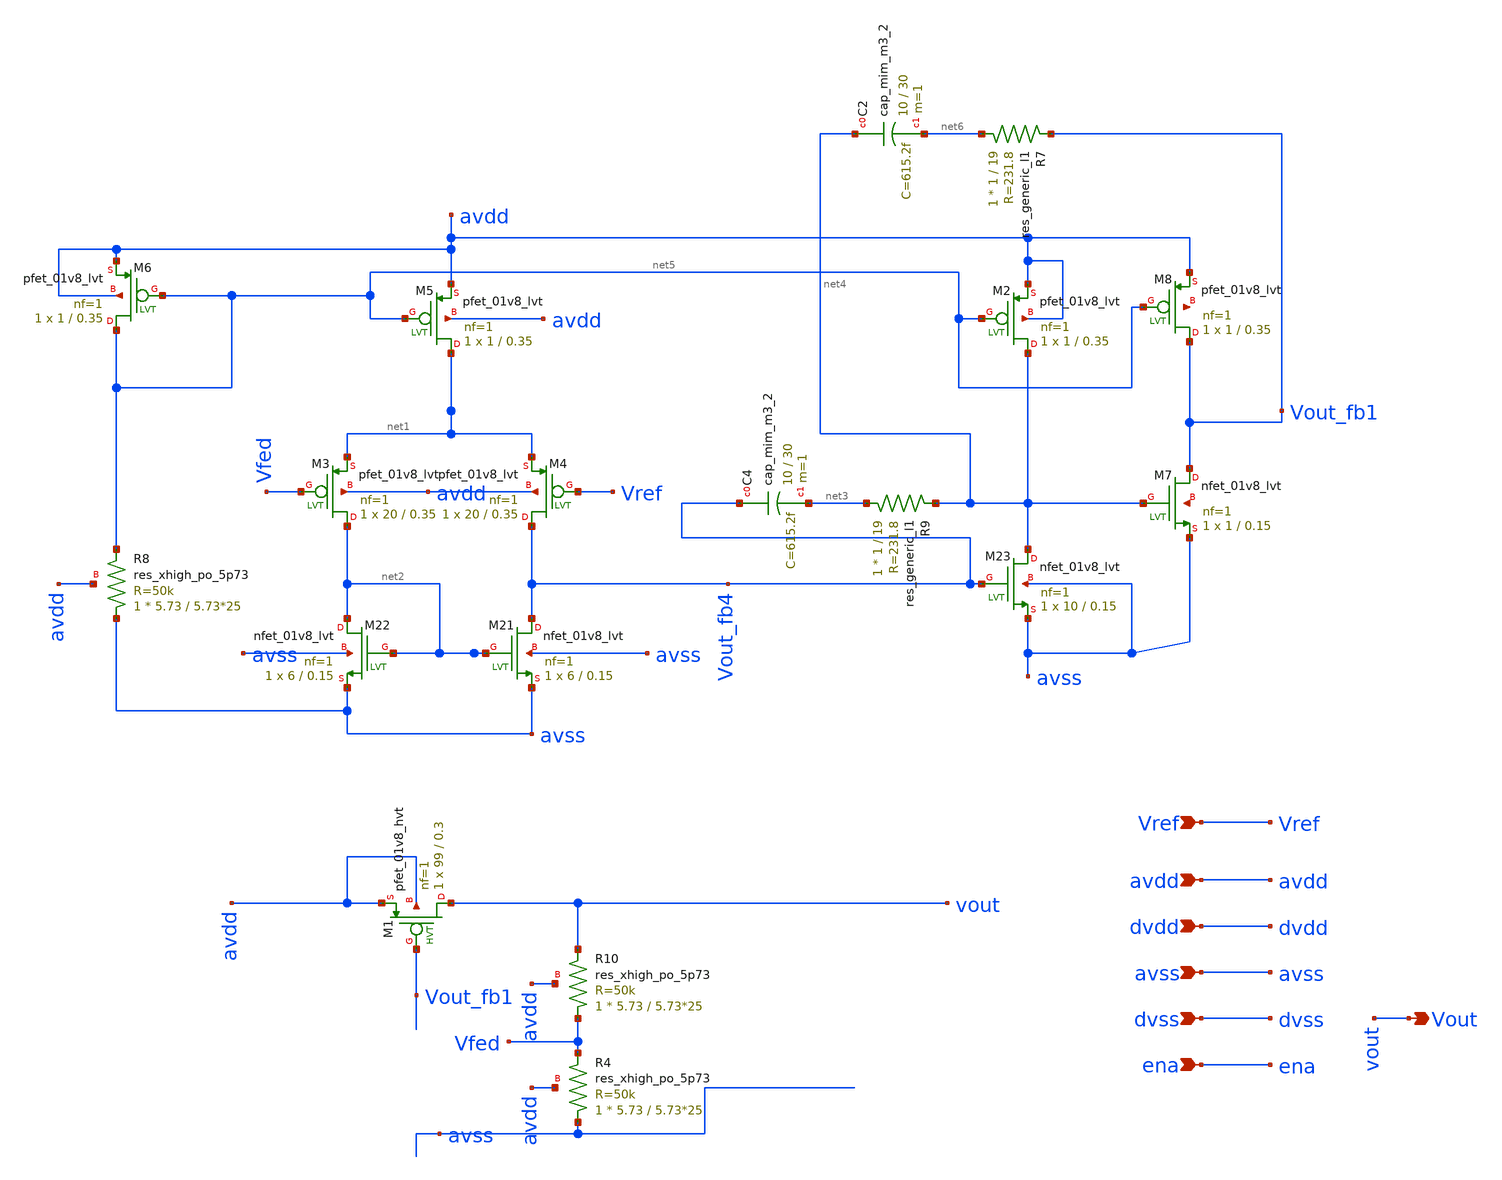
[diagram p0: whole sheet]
** sch_path: xschem/LDO_3.sch
**.subckt LDO_3 avdd dvss dvdd avss ena Vref Vout
*.ipin avdd
*.ipin dvss
*.ipin dvdd
*.ipin avss
*.ipin ena
*.ipin Vref
*.opin Vout
XM1 vout Vout_fb1 avdd avdd sky130_fd_pr__pfet_01v8_hvt L=0.3 W=99 nf=1 ad='int((nf+1)/2) * W/nf * 0.29'
+ as='int((nf+2)/2) * W/nf * 0.29' pd='2*int((nf+1)/2) * (W/nf + 0.29)' ps='2*int((nf+2)/2) * (W/nf + 0.29)'
+ nrd='0.29 / W' nrs='0.29 / W' sa=0 sb=0 sd=0 mult=1 m=1
XM21 Vout_fb4 net2 avss avss sky130_fd_pr__nfet_01v8_lvt L=0.15 W=6 nf=1 ad='int((nf+1)/2) * W/nf * 0.29'
+ as='int((nf+2)/2) * W/nf * 0.29' pd='2*int((nf+1)/2) * (W/nf + 0.29)' ps='2*int((nf+2)/2) * (W/nf + 0.29)'
+ nrd='0.29 / W' nrs='0.29 / W' sa=0 sb=0 sd=0 mult=1 m=1
XM22 net2 net2 avss avss sky130_fd_pr__nfet_01v8_lvt L=0.15 W=6 nf=1 ad='int((nf+1)/2) * W/nf * 0.29'
+ as='int((nf+2)/2) * W/nf * 0.29' pd='2*int((nf+1)/2) * (W/nf + 0.29)' ps='2*int((nf+2)/2) * (W/nf + 0.29)'
+ nrd='0.29 / W' nrs='0.29 / W' sa=0 sb=0 sd=0 mult=1 m=1
XM23 net4 Vout_fb4 avss avss sky130_fd_pr__nfet_01v8_lvt L=0.15 W=10 nf=1 ad='int((nf+1)/2) * W/nf * 0.29'
+ as='int((nf+2)/2) * W/nf * 0.29' pd='2*int((nf+1)/2) * (W/nf + 0.29)' ps='2*int((nf+2)/2) * (W/nf + 0.29)'
+ nrd='0.29 / W' nrs='0.29 / W' sa=0 sb=0 sd=0 mult=1 m=1
XM2 net4 net5 avdd avdd sky130_fd_pr__pfet_01v8_lvt L=0.35 W=1 nf=1 ad='int((nf+1)/2) * W/nf * 0.29'
+ as='int((nf+2)/2) * W/nf * 0.29' pd='2*int((nf+1)/2) * (W/nf + 0.29)' ps='2*int((nf+2)/2) * (W/nf + 0.29)'
+ nrd='0.29 / W' nrs='0.29 / W' sa=0 sb=0 sd=0 mult=1 m=1
XM3 net2 Vfed net1 avdd sky130_fd_pr__pfet_01v8_lvt L=0.35 W=20 nf=1 ad='int((nf+1)/2) * W/nf * 0.29'
+ as='int((nf+2)/2) * W/nf * 0.29' pd='2*int((nf+1)/2) * (W/nf + 0.29)' ps='2*int((nf+2)/2) * (W/nf + 0.29)'
+ nrd='0.29 / W' nrs='0.29 / W' sa=0 sb=0 sd=0 mult=1 m=1
XM4 Vout_fb4 Vref net1 avdd sky130_fd_pr__pfet_01v8_lvt L=0.35 W=20 nf=1 ad='int((nf+1)/2) * W/nf * 0.29'
+ as='int((nf+2)/2) * W/nf * 0.29' pd='2*int((nf+1)/2) * (W/nf + 0.29)' ps='2*int((nf+2)/2) * (W/nf + 0.29)'
+ nrd='0.29 / W' nrs='0.29 / W' sa=0 sb=0 sd=0 mult=1 m=1
XM5 net1 net5 avdd avdd sky130_fd_pr__pfet_01v8_lvt L=0.35 W=1 nf=1 ad='int((nf+1)/2) * W/nf * 0.29'
+ as='int((nf+2)/2) * W/nf * 0.29' pd='2*int((nf+1)/2) * (W/nf + 0.29)' ps='2*int((nf+2)/2) * (W/nf + 0.29)'
+ nrd='0.29 / W' nrs='0.29 / W' sa=0 sb=0 sd=0 mult=1 m=1
XM6 net5 net5 avdd avdd sky130_fd_pr__pfet_01v8_lvt L=0.35 W=1 nf=1 ad='int((nf+1)/2) * W/nf * 0.29'
+ as='int((nf+2)/2) * W/nf * 0.29' pd='2*int((nf+1)/2) * (W/nf + 0.29)' ps='2*int((nf+2)/2) * (W/nf + 0.29)'
+ nrd='0.29 / W' nrs='0.29 / W' sa=0 sb=0 sd=0 mult=1 m=1
XM7 Vout_fb1 net4 avss net7 sky130_fd_pr__nfet_01v8_lvt L=0.15 W=1 nf=1 ad='int((nf+1)/2) * W/nf * 0.29'
+ as='int((nf+2)/2) * W/nf * 0.29' pd='2*int((nf+1)/2) * (W/nf + 0.29)' ps='2*int((nf+2)/2) * (W/nf + 0.29)'
+ nrd='0.29 / W' nrs='0.29 / W' sa=0 sb=0 sd=0 mult=1 m=1
XM8 Vout_fb1 net5 avdd net8 sky130_fd_pr__pfet_01v8_lvt L=0.35 W=1 nf=1 ad='int((nf+1)/2) * W/nf * 0.29'
+ as='int((nf+2)/2) * W/nf * 0.29' pd='2*int((nf+1)/2) * (W/nf + 0.29)' ps='2*int((nf+2)/2) * (W/nf + 0.29)'
+ nrd='0.29 / W' nrs='0.29 / W' sa=0 sb=0 sd=0 mult=1 m=1
XR8 avss net5 avdd sky130_fd_pr__res_xhigh_po_5p73 L=5.73*25 mult=1 m=1
XC4 Vout_fb4 net3 sky130_fd_pr__cap_mim_m3_2 W=10 L=30 MF=1 m=1
R9 net3 net4 sky130_fd_pr__res_generic_l1 W=1 L=19 m=1
XC2 net4 net6 sky130_fd_pr__cap_mim_m3_2 W=10 L=30 MF=1 m=1
R7 net6 Vout_fb1 sky130_fd_pr__res_generic_l1 W=1 L=19 m=1
XR10 Vfed vout avdd sky130_fd_pr__res_xhigh_po_5p73 L=5.73*25 mult=1 m=1
XR4 avss Vfed avdd sky130_fd_pr__res_xhigh_po_5p73 L=5.73*25 mult=1 m=1
**.ends
.end
